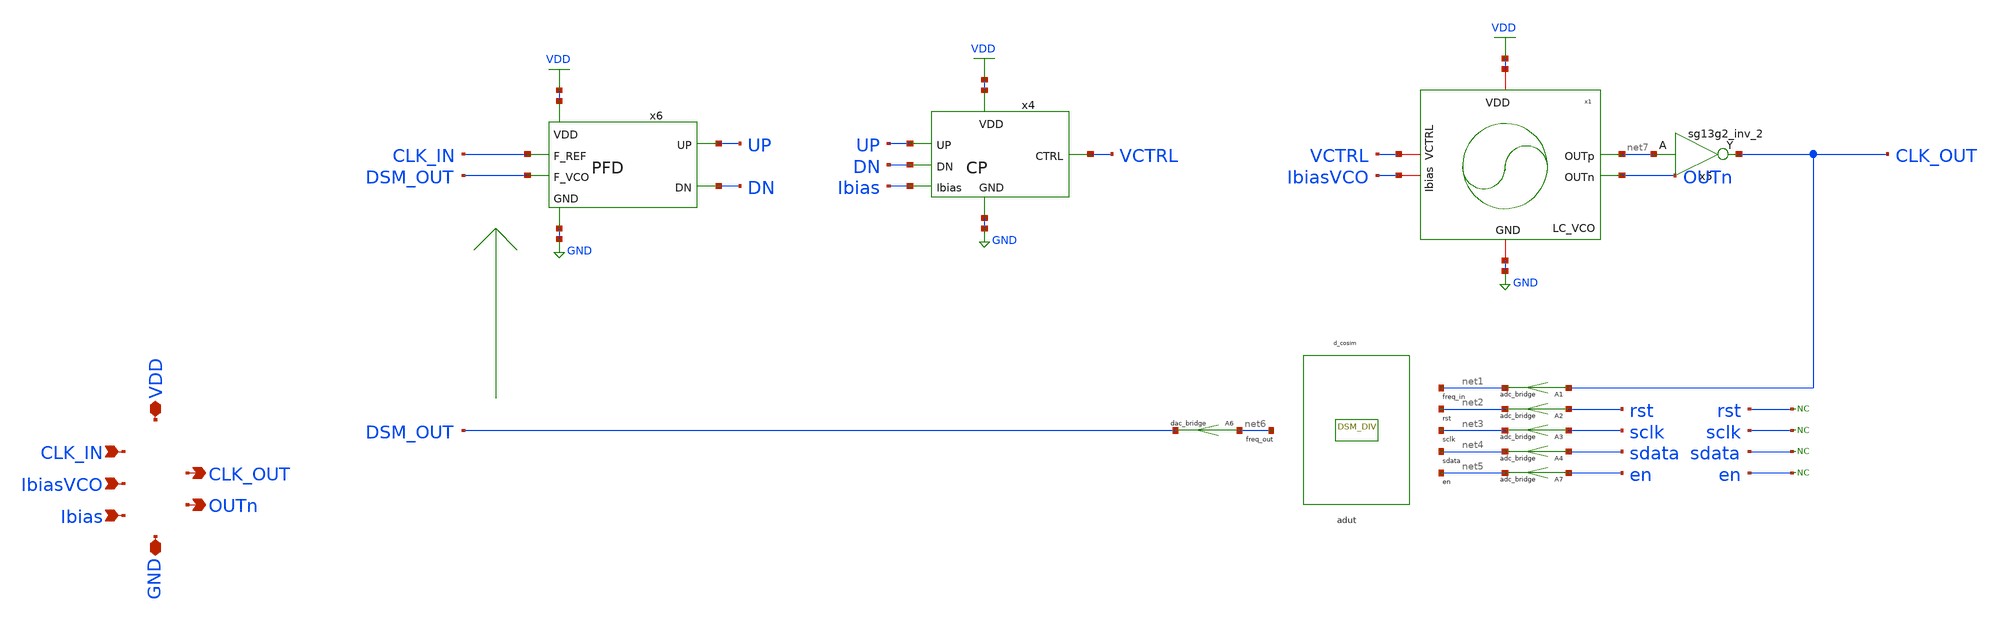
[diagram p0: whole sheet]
** sch_path: schematic/top-pll/LC_VCO_PLL.sch
**.subckt LC_VCO_PLL GND VDD CLK_IN IbiasVCO Ibias OUTn CLK_OUT
*.iopin GND
*.iopin VDD
*.ipin CLK_IN
*.ipin IbiasVCO
*.ipin Ibias
*.opin OUTn
*.opin CLK_OUT
x5 CLK_OUT net7 VDD GND sg13g2_inv_2
* noconn rst
* noconn sclk
* noconn sdata
* noconn en
x4 VDD UP VCTRL DN GND Ibias CP
x6 VDD UP CLK_IN DSM_OUT DN GND PFD
x1 VDD net7 OUTn IbiasVCO VCTRL GND LC_VCO
adut [ net1 net2 net3 net4 net5 ] [ net6 ] null dut
.model dut d_cosim simulation=./../dsm_and_freq_divider.so
A1 [ CLK_OUT ] [ net1 ] adc1
.model adc1 adc_bridge in_low=0.76 in_high=0.76
A6 [ net6 ] [ DSM_OUT ] dac1
.model dac1 dac_bridge out_low=0 out_high=1.2
A7 [ en ] [ net5 ] adc1
.model adc1 adc_bridge in_low=0.76 in_high=0.76
A2 [ rst ] [ net2 ] adc1
.model adc1 adc_bridge in_low=0.76 in_high=0.76
A3 [ sclk ] [ net3 ] adc1
.model adc1 adc_bridge in_low=0.76 in_high=0.76
A4 [ sdata ] [ net4 ] adc1
.model adc1 adc_bridge in_low=0.76 in_high=0.76
**.ends
.GLOBAL VDD
.GLOBAL GND
.end
